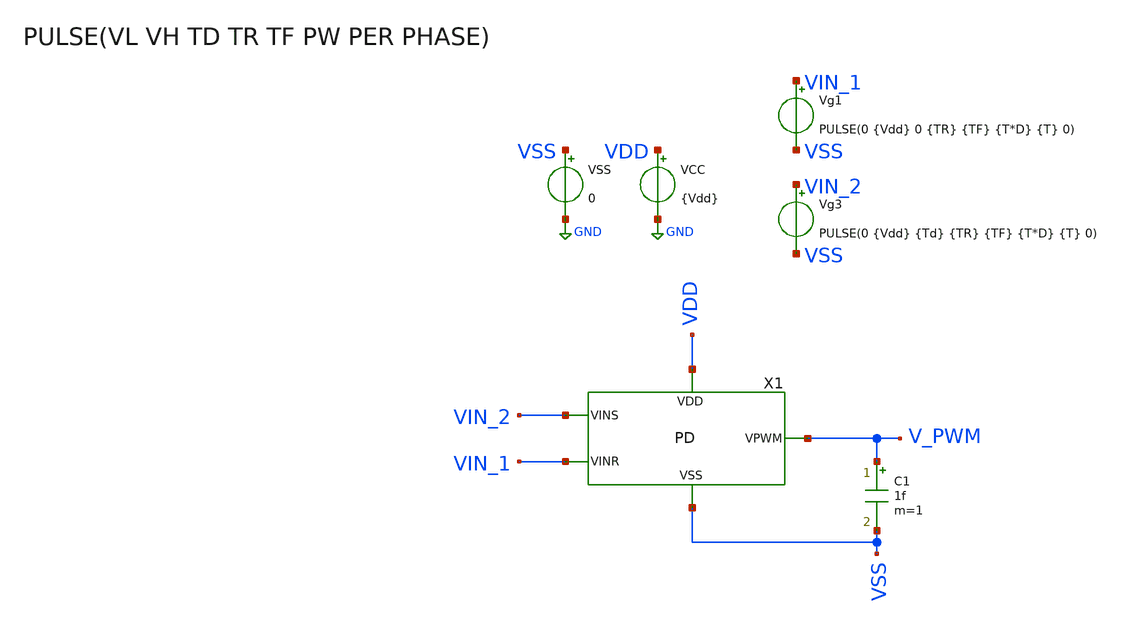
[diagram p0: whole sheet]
** sch_path: xschem/PD/TB_PhaseDetector.sch
**.subckt TB_PhaseDetector
VCC VDD GND {Vdd}
VSS VSS GND 0
Vg1 VIN_1 VSS PULSE(0 {Vdd} 0 {TR} {TF} {T*D} {T} 0)
Vg3 VIN_2 VSS PULSE(0 {Vdd} {Td} {TR} {TF} {T*D} {T} 0)
C1 V_PWM VSS 1f m=1
X1 V_PWM VIN_2 VDD VSS VIN_1 PD
**** begin user architecture code


.param Vdd = 1.2
.param VH = 1.2
.param Del = 0

.param Vcont = 0

.param fsw = 10Meg
.param T = 1/fsw
.csparam T = {T}
.param TR = 1p
.param TF = 1p

* Pulse width
.param PW = 1n
.param C_del= 0.1p
.param R_del = PW/C_del

*Caso 1 - Funciona bien
.param D = 0.5
.param Td = T*0.3






.param temp = 27





.save all
.tran 100p {5*T}
.control
set color0 = white
run
plot v(VIN_1) v(VIN_2)+2 v(V_PWM)+4
plot v(VIN_1) v(x1.VP1)+2
plot v(VIN_2) v(x1.VP2)+2
*plot v(X) v(Y)+2 v(VIN_S)+4
.endc

*.measure tran tdead_fall
*+ TRIG tran1.V(vcn) TD=0u VAL=0.9 FALL=1
*+ TARG tran1.V(vcp) TD=0u VAL=0.9 FALL=1

*.measure tran t_large_delay
*+ TRIG tran1.V(x1.C1) TD=0u VAL=0.9 RISE=1
*+ TARG tran1.V(x1.B2) TD=0u VAL=0.9 RISE=1





.param temp=27
.param mult = 1

.param w_P_NOR =0.15u
.param l_P_NOR = 0.15u

.param w_N_NOR =0.15u
.param l_N_NOR =0.15u

.param w_inv =0.15u
.param l_inv =0.15u






.param temp=27
.param mult = 1

.param w_P_AND =0.15u
.param l_P_AND = 0.15u

.param w_N_AND =0.15u
.param l_N_AND =0.15u








.lib cornerMOShv.lib mos_tt
.lib cornerMOSlv.lib mos_tt
*.lib cornerMOShv.lib mos_ff
*.lib cornerMOSlv.lib mos_ff
*.lib cornerMOShv.lib mos_ss
*.lib cornerMOSlv.lib mos_ss
*.lib cornerMOShv.lib mos_sf
*.lib cornerMOSlv.lib mos_sf
*.lib cornerMOShv.lib mos_fs
*.lib cornerMOSlv.lib mos_fs

*.include /opt/pdks/ihp-sg13g2/libs.ref/sg13g2_stdcell/spice/sg13g2_stdcell.spice
*.lib $::SG13G2_MODELS/cornerRES.lib res_typ
*.lib $::SG13G2_MODELS/cornerCAP.lib cap_typ
*.lib $::SG13G2_MODELS/diodes.lib

**** end user architecture code
**.ends

* expanding   symbol:  ../PD/PD.sym # of pins=5
** sym_path: xschem/PD/PD.sym
** sch_path: xschem/PD/PD.sch
.subckt PD VPWM VINS VDD VSS VINR
*.iopin VDD
*.ipin VINR
*.opin VPWM
*.iopin VSS
*.ipin VINS
X1 VPWM VP1 VDD VSS VP2 SR_Latch
X2 VP1 VINR VDD VSS SPG
X3 VP2 VINS VDD VSS SPG
**** begin user architecture code



**** end user architecture code
.ends


* expanding   symbol:  ../SR_Latch_NOR/SR_Latch.sym # of pins=5
** sym_path: xschem/SR_Latch_NOR/SR_Latch.sym
** sch_path: xschem/SR_Latch_NOR/SR_Latch.sch
.subckt SR_Latch VPWM VINS VDD VSS VINR
*.iopin VDD
*.ipin VINS
*.iopin VSS
*.opin VPWM
*.ipin VINR
X1 VDD VSS V_N VINS VPWM NOR
X2 VDD VSS VPWM V_N VINR NOR
**** begin user architecture code



**** end user architecture code
.ends


* expanding   symbol:  ../SPG/SPG.sym # of pins=4
** sym_path: xschem/SPG/SPG.sym
** sch_path: xschem/SPG/SPG.sch
.subckt SPG VP Vin VDD VSS
*.iopin VDD
*.ipin Vin
*.opin VP
*.iopin VSS
R1 B1 net1 {R_del} m=1
C4 B1 VSS {C_del} m=1
X1 Vin net3 VDD VSS INV
X2 A B VSS VDD VP AND
X3 net3 B VDD VSS INV
X4 B net1 VDD VSS INV
X5 B1 net2 VDD VSS INV
X6 net2 A VDD VSS INV
**** begin user architecture code



**** end user architecture code
.ends


* expanding   symbol:  ../DigitalGates/NOR.sym # of pins=5
** sym_path: xschem/DigitalGates/NOR.sym
** sch_path: xschem/DigitalGates/NOR.sch
.subckt NOR VDD VSS F X Y
*.iopin VDD
*.ipin X
*.opin F
*.iopin VSS
*.ipin Y
XM1 F Y VSS VSS sg13_lv_nmos w={w_N_NOR} l={l_N_NOR} ng=1 m={mult} mm_ok=1
XM2 net1 X VDD VDD sg13_lv_pmos w={w_P_NOR} l={l_P_NOR} ng=1 m={mult*3} mm_ok=1
XM4 F Y net1 VDD sg13_lv_pmos w={w_P_NOR} l={l_P_NOR} ng=1 m={mult*3} mm_ok=1
XM3 F X VSS VSS sg13_lv_nmos w={w_N_NOR} l={l_N_NOR} ng=1 m={mult} mm_ok=1
**** begin user architecture code



**** end user architecture code
.ends


* expanding   symbol:  ../DigitalGates/INV.sym # of pins=4
** sym_path: xschem/DigitalGates/INV.sym
** sch_path: xschem/DigitalGates/INV.sch
.subckt INV X Y VDD VSS
*.iopin VDD
*.ipin X
*.opin Y
*.iopin VSS
XM3 Y X VSS VSS sg13_lv_nmos w={w_inv} l={l_inv} ng=1 m={mult} mm_ok=1
XM4 Y X VDD VDD sg13_lv_pmos w={w_inv} l={l_inv} ng=1 m={mult*3} mm_ok=1
**** begin user architecture code



**** end user architecture code
.ends


* expanding   symbol:  ../DigitalGates/AND.sym # of pins=5
** sym_path: xschem/DigitalGates/AND.sym
** sch_path: xschem/DigitalGates/AND.sch
.subckt AND X Y VSS VDD F
*.iopin VDD
*.ipin X
*.opin F
*.iopin VSS
*.ipin Y
XM1 net1 X net2 VSS sg13_lv_nmos w={w_N_AND} l={l_N_AND} ng=1 m={mult} mm_ok=1
XM2 F net1 VDD VDD sg13_lv_pmos w={w_P_AND} l={l_P_AND} ng=1 m={mult*3} mm_ok=1
XM3 net2 Y VSS VSS sg13_lv_nmos w={w_N_AND} l={l_N_AND} ng=1 m={mult} mm_ok=1
XM4 F net1 VSS VSS sg13_lv_nmos w={w_N_AND} l={l_N_AND} ng=1 m={mult} mm_ok=1
XM5 net1 Y VDD VDD sg13_lv_pmos w={w_P_AND} l={l_P_AND} ng=1 m={mult*3} mm_ok=1
XM6 net1 X VDD VDD sg13_lv_pmos w={w_P_AND} l={l_P_AND} ng=1 m={mult*3} mm_ok=1
**** begin user architecture code



**** end user architecture code
.ends

.GLOBAL GND
.end
